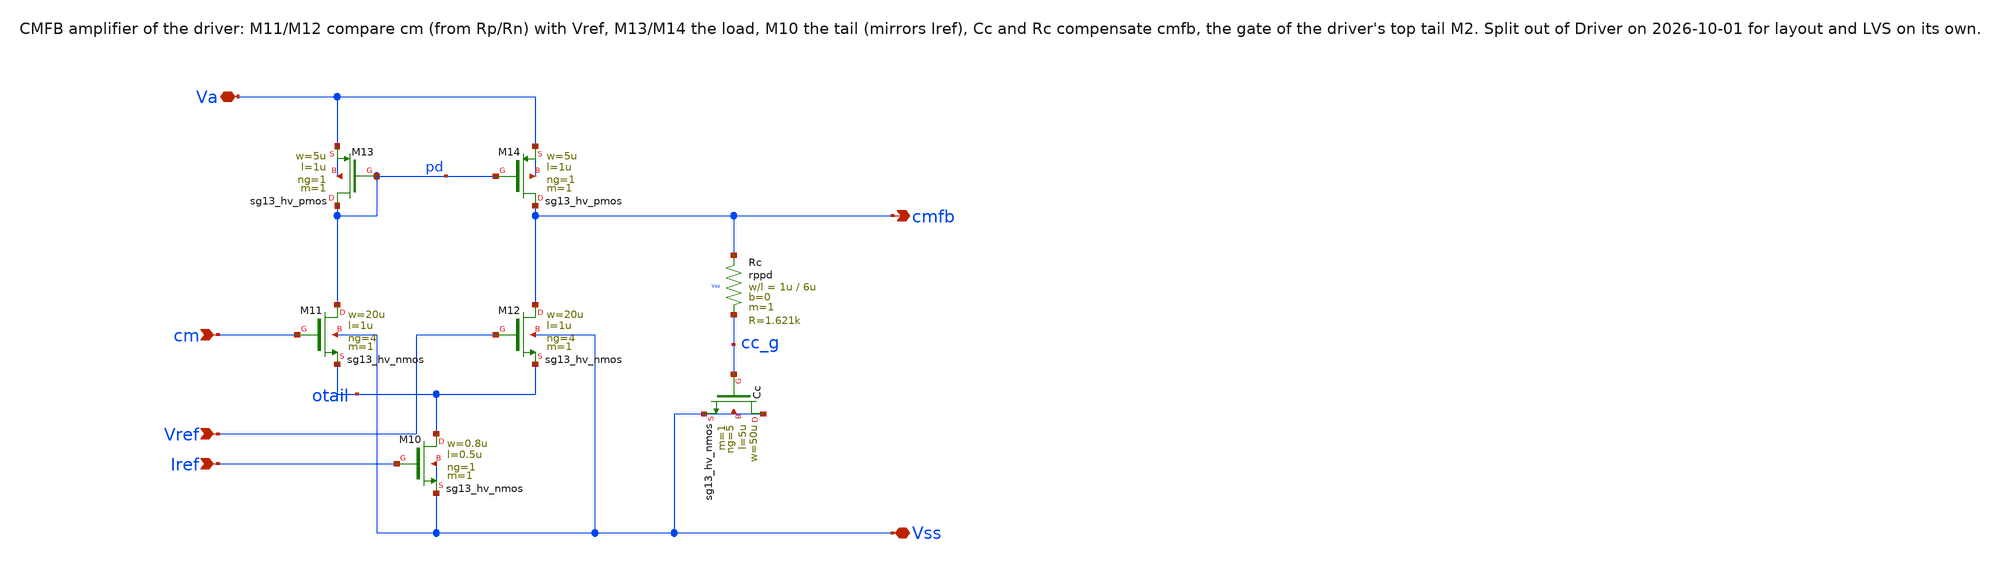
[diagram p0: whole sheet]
** sch_path: macros/lvds_tx/schematic/xschem/cmfb_amp.sch
**.subckt cmfb_amp Va Vss cm Iref Vref cmfb
*.iopin Va
*.iopin Vss
*.ipin cm
*.ipin Iref
*.ipin Vref
*.opin cmfb
XM13 pd pd Va Va sg13_hv_pmos w=5u l=1u ng=1 m=1 mm_ok=1
XM14 cmfb pd Va Va sg13_hv_pmos w=5u l=1u ng=1 m=1 mm_ok=1
XM11 pd cm otail Vss sg13_hv_nmos w=20u l=1u ng=4 m=1 mm_ok=1
XM12 cmfb Vref otail Vss sg13_hv_nmos w=20u l=1u ng=4 m=1 mm_ok=1
XM10 otail Iref Vss Vss sg13_hv_nmos w=0.8u l=0.5u ng=1 m=1 mm_ok=1
XCc Vss cc_g Vss Vss sg13_hv_nmos w=50u l=5u ng=5 m=1 mm_ok=1
XRc cmfb cc_g Vss rppd w=1u l=6u m=1 b=0 mm_ok=1
**.ends
.end
